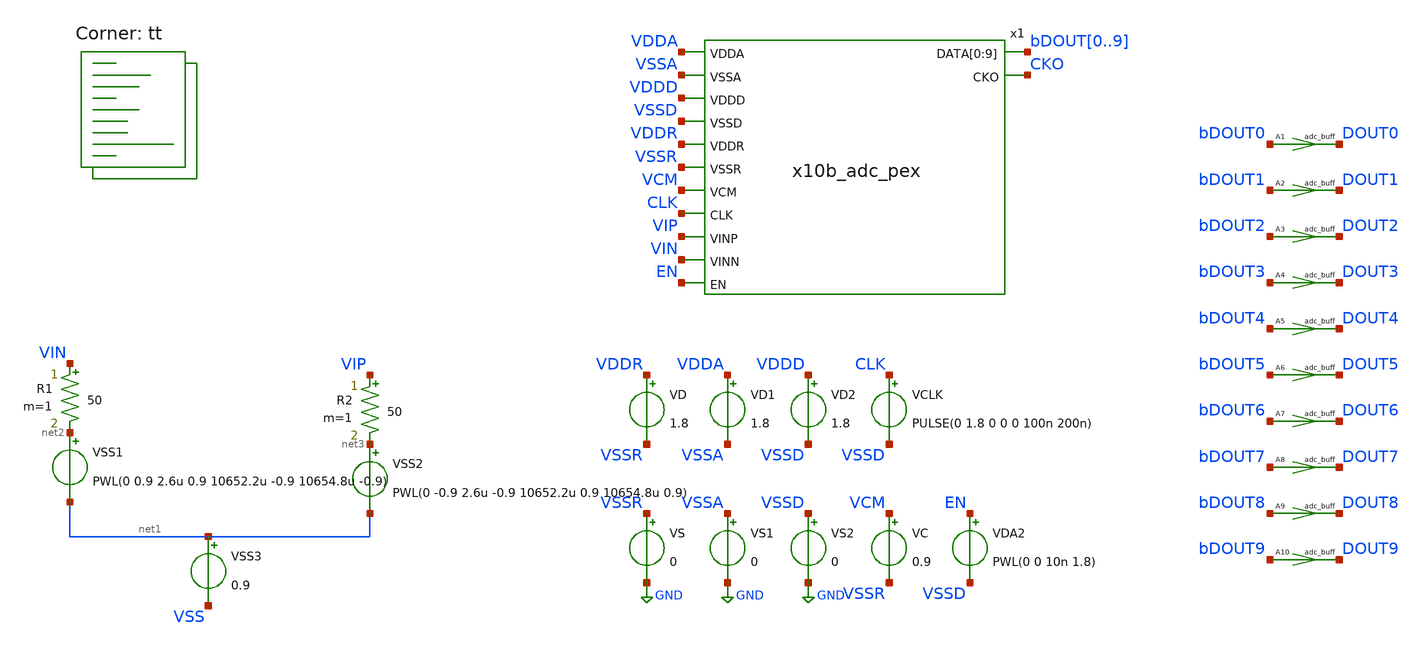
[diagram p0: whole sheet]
** sch_path: xschem/adc_tb_static.pex.sch
**.subckt adc_tb_static.pex
VSS1 net2 net1 PWL(0 0.9 2.6u 0.9 10652.2u -0.9 10654.8u -0.9)
VSS2 net3 net1 PWL(0 -0.9 2.6u -0.9 10652.2u 0.9 10654.8u 0.9)
VSS3 net1 VSS 0.9
R1 VIN net2 50 m=1
R2 VIP net3 50 m=1
A1 [ bDOUT0 ] [ DOUT0 ] adc_buff
A2 [ bDOUT1 ] [ DOUT1 ] adc_buff
A3 [ bDOUT2 ] [ DOUT2 ] adc_buff
A4 [ bDOUT3 ] [ DOUT3 ] adc_buff
A5 [ bDOUT4 ] [ DOUT4 ] adc_buff
A6 [ bDOUT5 ] [ DOUT5 ] adc_buff
A7 [ bDOUT6 ] [ DOUT6 ] adc_buff
A8 [ bDOUT7 ] [ DOUT7 ] adc_buff
A9 [ bDOUT8 ] [ DOUT8 ] adc_buff
A10 [ bDOUT9 ] [ DOUT9 ] adc_buff
VS VSSR GND 0
VD VDDR VSSR 1.8
VCLK CLK VSSD PULSE(0 1.8 0 0 0 100n 200n)
x1 VDDA VSSA VDDD VSSD VDDR VSSR VCM CLK VIP VIN EN bDOUT0 bDOUT1 bDOUT2 bDOUT3 bDOUT4 bDOUT5 bDOUT6
+ bDOUT7 bDOUT8 bDOUT9 CKO x10b_adc_pex
VC VCM VSSR 0.9
VDA2 EN VSSD PWL(0 0 10n 1.8)
VS1 VSSA GND 0
VD1 VDDA VSSA 1.8
VS2 VSSD GND 0
VD2 VDDD VSSD 1.8
**** begin user architecture code

** opencircuitdesign pdks install
* .lib $::SKYWATER_MODELS/sky130.lib.spice tt
*.include $PDK_ROOT/$PDK/libs.ref/sky130_fd_sc_hdll/spice/sky130_fd_sc_hdll.spice
.include $PDK_ROOT/$PDK/libs.ref/sky130_fd_sc_hs/spice/sky130_fd_sc_hs.spice
*.include $PDK_ROOT/$PDK/libs.ref/sky130_fd_sc_hd/spice/sky130_fd_sc_hd.spice

.lib $::SKYWATER_MODELS/sky130.lib.spice tt


.option wnflag=0 bypass=1
.options method=trap rawfile=binary
.options solver=klu nomod
Eout out 0 VALUE = { ((V(dout0)*512 + V(dout1)*256 + V(dout2)*128 + V(dout3)*64 + V(dout4)*32 + V(dout5)*16 + V(dout6)*8 + V(dout7)*4 + V(dout8)*2 + V(dout9)*1)/3.3) - 512 }
Epowa pow_a 0 VALUE = { V(vdda)*(-i(vd1)) }
Epowd pow_d 0 VALUE = { V(vddd)*(-i(vd2)) }
Epowr pow_r 0 VALUE = { V(vddr)*(-i(vd)) }
.model adc_buff adc_bridge(in_low=0.18 in_high=1.62 rise_delay=100p fall_delay=100p)
.control
global netlist_dir .
set num_threads=16
save cko out pow_a pow_d pow_r vip vin x1.th_dif_sw_0.VCP x1.th_dif_sw_0.VCN
tran 1n 5350u 0 uic; Mengubah start time menjadi 10n
rusage traniter trantime
meas tran avg_pow  AVG pow_a from=1n to=535u
meas tran avg_pow  AVG pow_d from=1n to=535u
meas tran avg_pow  AVG pow_r from=1n to=535u
remzerovec
write adc10b_tb_static_pex.raw
wrdata adc10b_tb_static_pex.txt out cko pow_a pow_d pow_r vip vin
quit 1
.endc


**** end user architecture code
**.ends

* expanding   symbol:  x10b_adc_pex.sym # of pins=13
** sym_path: xschem/x10b_adc_pex.sym
.include /home/mthudaa/vlsi/8bit_SAR-ADC_ITS/xschem/x10b_adc_pex.spice
.GLOBAL GND
.end
